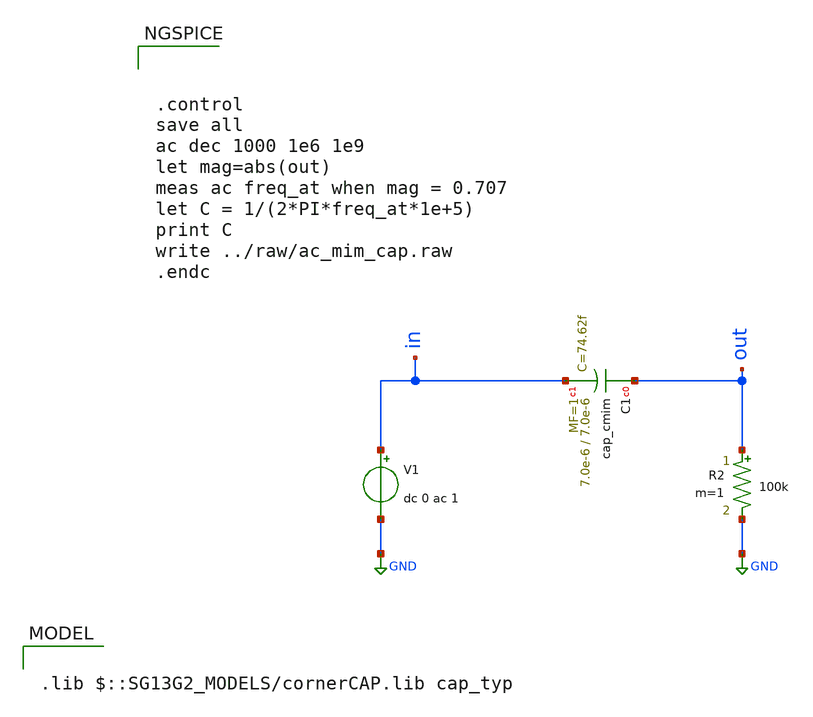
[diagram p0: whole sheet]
** sch_path: ihp-sg13g2/libs.tech/xschem/sg13g2_tests/ac_mim_cap.sch
* Copyright 2021 Stefan Frederik Schippers
* Licensed under the Apache License, Version 2.0 (the "License");
* you may not use this file except in compliance with the License.
* You may obtain a copy of the License at
* https://www.apache.org/licenses/LICENSE-2.0
* Unless required by applicable law or agreed to in writing, software
* distributed under the License is distributed on an "AS IS" BASIS,
* WITHOUT WARRANTIES OR CONDITIONS OF ANY KIND, either express or implied.
* See the License for the specific language governing permissions and
* limitations under the License.
* Copyright 2023 IHP PDK Authors
**.subckt ac_mim_cap
V1 in GND dc 0 ac 1
R2 out GND 100k m=1
XC1 out in cap_cmim W=7.0e-6 L=7.0e-6 MF=1
**** begin user architecture code



.control
save all
ac dec 1000 1e6 1e9
let mag=abs(out)
meas ac freq_at when mag = 0.707
let C = 1/(2*PI*freq_at*1e+5)
print C
write ../raw/ac_mim_cap.raw
.endc



.lib $::SG13G2_MODELS/cornerCAP.lib cap_typ

**** end user architecture code
**.ends
.GLOBAL GND
.end
